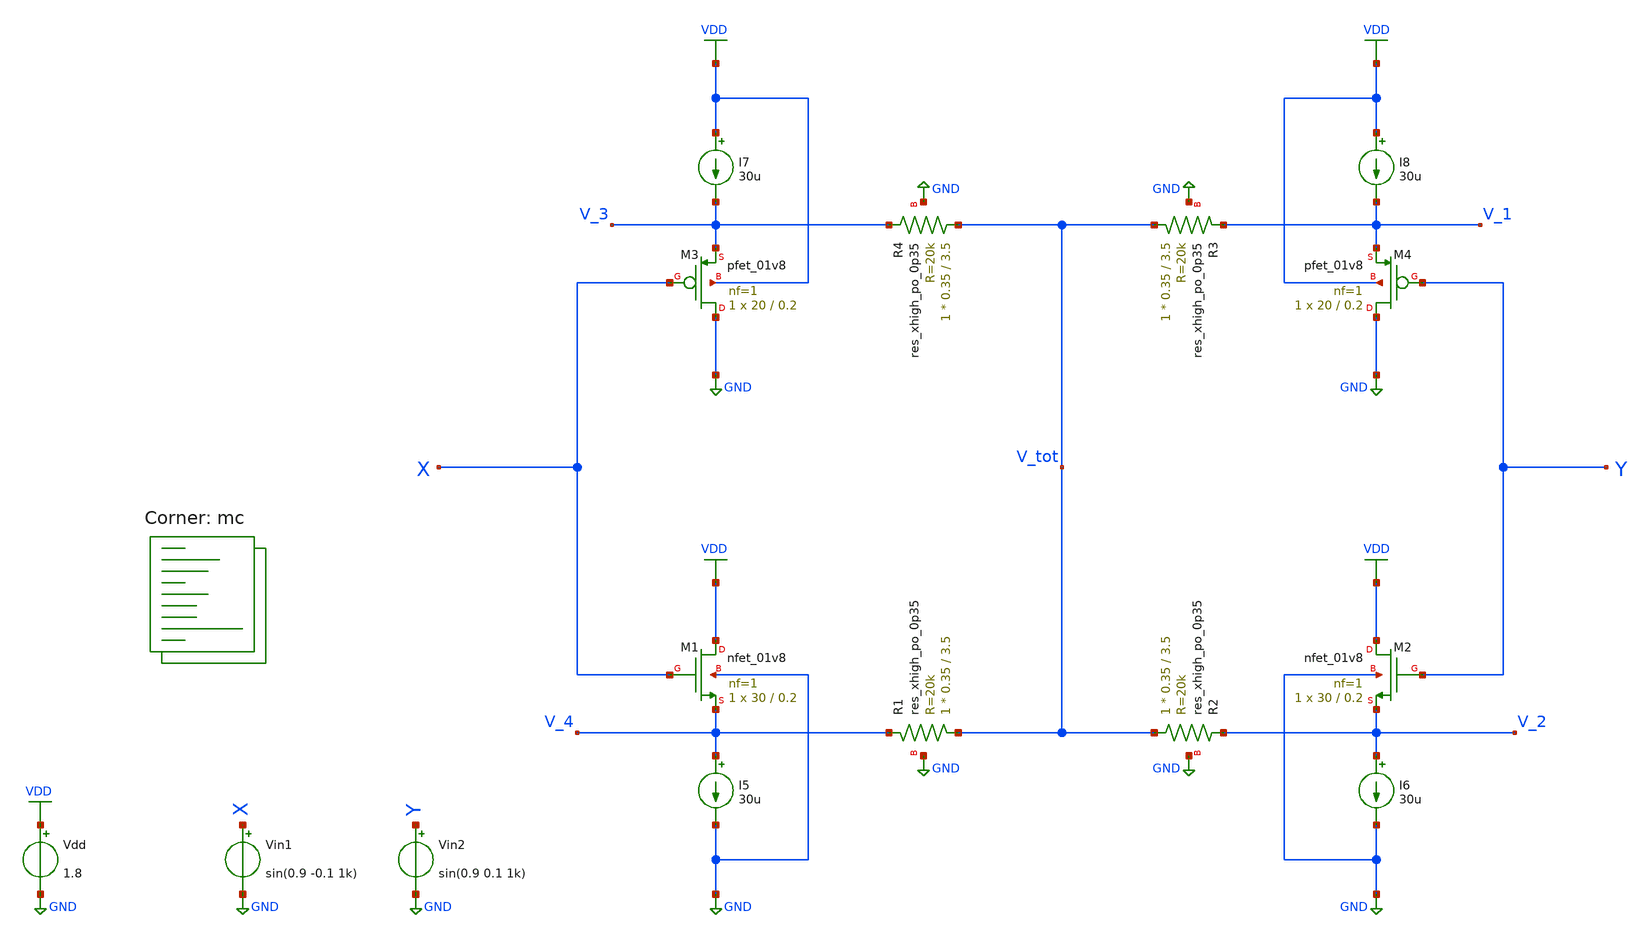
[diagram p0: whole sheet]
** sch_path: projects/montecarlo/xschem_ngspice/inverter/CMFB_mc.sch
**.subckt CMFB_mc
Vdd VDD GND 1.8
XM1 VDD X V_4 GND sky130_fd_pr__nfet_01v8 L=0.2 W=30 nf=1 ad='int((nf+1)/2) * W/nf * 0.29' as='int((nf+2)/2) * W/nf * 0.29'
+ pd='2*int((nf+1)/2) * (W/nf + 0.29)' ps='2*int((nf+2)/2) * (W/nf + 0.29)' nrd='0.29 / W' nrs='0.29 / W'
+ sa=0 sb=0 sd=0 mult=1 m=1
XM3 GND X V_3 VDD sky130_fd_pr__pfet_01v8 L=0.2 W=20 nf=1 ad='int((nf+1)/2) * W/nf * 0.29' as='int((nf+2)/2) * W/nf * 0.29'
+ pd='2*int((nf+1)/2) * (W/nf + 0.29)' ps='2*int((nf+2)/2) * (W/nf + 0.29)' nrd='0.29 / W' nrs='0.29 / W'
+ sa=0 sb=0 sd=0 mult=1 m=1
XM2 VDD Y V_2 GND sky130_fd_pr__nfet_01v8 L=0.2 W=30 nf=1 ad='int((nf+1)/2) * W/nf * 0.29' as='int((nf+2)/2) * W/nf * 0.29'
+ pd='2*int((nf+1)/2) * (W/nf + 0.29)' ps='2*int((nf+2)/2) * (W/nf + 0.29)' nrd='0.29 / W' nrs='0.29 / W'
+ sa=0 sb=0 sd=0 mult=1 m=1
XM4 GND Y V_1 VDD sky130_fd_pr__pfet_01v8 L=0.2 W=20 nf=1 ad='int((nf+1)/2) * W/nf * 0.29' as='int((nf+2)/2) * W/nf * 0.29'
+ pd='2*int((nf+1)/2) * (W/nf + 0.29)' ps='2*int((nf+2)/2) * (W/nf + 0.29)' nrd='0.29 / W' nrs='0.29 / W'
+ sa=0 sb=0 sd=0 mult=1 m=1
I5 V_4 GND 30u
I6 V_2 GND 30u
I7 VDD V_3 30u
I8 VDD V_1 30u
Vin1 X GND sin(0.9 -0.1 1k)
Vin2 Y GND sin(0.9 0.1 1k)
XR1 V_tot V_4 GND sky130_fd_pr__res_xhigh_po_0p35 L=3.5 mult=1 m=1
XR2 V_tot V_2 GND sky130_fd_pr__res_xhigh_po_0p35 L=3.5 mult=1 m=1
XR3 V_tot V_1 GND sky130_fd_pr__res_xhigh_po_0p35 L=3.5 mult=1 m=1
XR4 V_tot V_3 GND sky130_fd_pr__res_xhigh_po_0p35 L=3.5 mult=1 m=1
**** begin user architecture code



.option wnflag=1
.option savecurrents
.save @m.xm1.msky130_fd_pr__nfet_01v8[gm] @m.xm1.msky130_fd_pr__nfet_01v8[vth] @m.xm2.msky130_fd_pr__nfet_01v8[gm] @m.xm3.msky130_fd_pr__nfet_01v8[vth] @m.xm3.msky130_fd_pr__pfet_01v8[gm] @m.xm3.msky130_fd_pr__pfet_01v8[vth] @m.xm4.msky130_fd_pr__pfet_01v8[gm] @m.xm4.msky130_fd_pr__pfet_01v8[vth]

.control

  let runs=20
  let run=1

  dowhile run <= runs
    save all
    * dc vin 0 1.8 0.01
    tran 1u 3m
    write CMFB_mc.raw
    set appendwrite
    reset
    let run = run + 1
  end

.endc



.lib $::SKYWATER_MODELS/sky130.lib.spice mc
**** end user architecture code
**.ends
.GLOBAL GND
.GLOBAL VDD
.end
